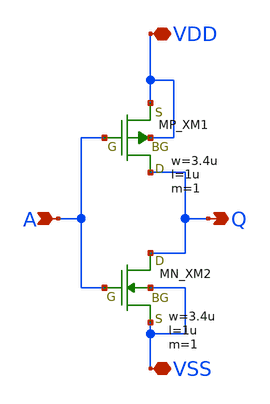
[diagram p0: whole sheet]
** sch_path: member_project/inverter/ichiken/Luft256/inverter_Luft256.sch
**.subckt inverter_Luft256 A VDD VSS Q
*.ipin A
*.iopin VDD
*.iopin VSS
*.opin Q
XM1 Q A VDD VDD PMOS w=3.4u l=1u as=0 ad=0 ps=0 pd=0 nrd=0 nrs=0 m=1
XM2 Q A VSS VSS NMOS w=3.4u l=1u as=0 ad=0 ps=0 pd=0 nrd=0 nrs=0 m=1
**.ends
.end
